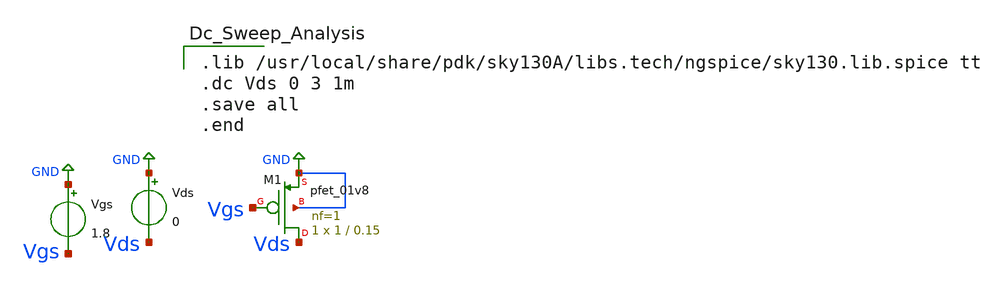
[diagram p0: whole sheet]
** sch_path: Schematics/pmos_analysis.sch
**.subckt pmos_analysis
Vgs GND Vgs 1.8
XM1 Vds Vgs GND GND sky130_fd_pr__pfet_01v8 L=0.15 W=1 nf=1 ad='int((nf+1)/2) * W/nf * 0.29' as='int((nf+2)/2) * W/nf * 0.29'
+ pd='2*int((nf+1)/2) * (W/nf + 0.29)' ps='2*int((nf+2)/2) * (W/nf + 0.29)' nrd='0.29 / W' nrs='0.29 / W'
+ sa=0 sb=0 sd=0 mult=1 m=1
Vds GND Vds 0
**** begin user architecture code

.lib /usr/local/share/pdk/sky130A/libs.tech/ngspice/sky130.lib.spice tt
.dc Vds 0 3 1m
.save all
.end

**** end user architecture code
**.ends
.GLOBAL GND
.end
